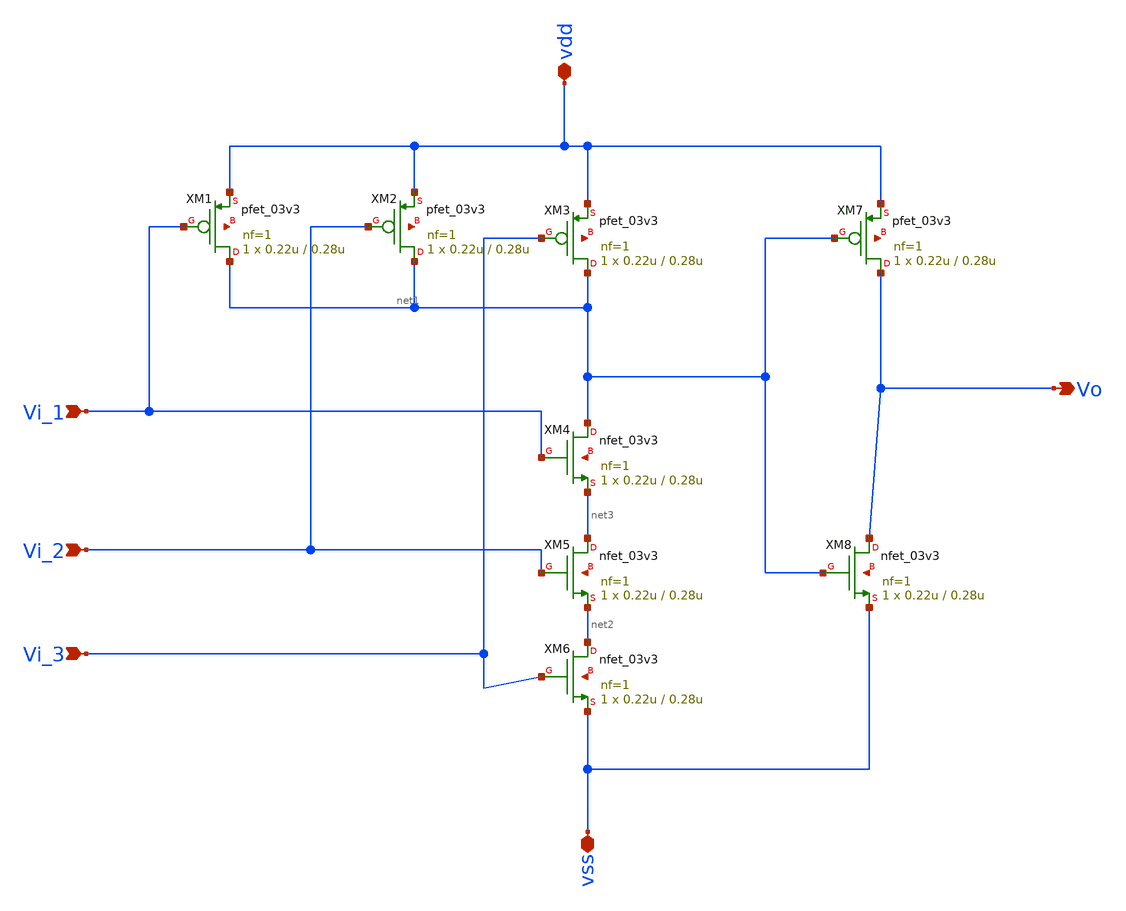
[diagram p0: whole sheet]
** sch_path: designs/3_input_and.sch
**.subckt 3_input_and vdd vss Vi_1 Vi_2 Vi_3 Vo
*.iopin vdd
*.iopin vss
*.ipin Vi_1
*.ipin Vi_2
*.ipin Vi_3
*.opin Vo
XM1 net1 Vi_1 vdd net4 pfet_03v3 L=0.28u W=0.22u nf=1 ad='int((nf+1)/2) * W/nf * 0.18u' as='int((nf+2)/2) * W/nf * 0.18u'
+ pd='2*int((nf+1)/2) * (W/nf + 0.18u)' ps='2*int((nf+2)/2) * (W/nf + 0.18u)' nrd='0.18u / W' nrs='0.18u / W'
+ sa=0 sb=0 sd=0 m=1
XM2 net1 Vi_2 vdd net5 pfet_03v3 L=0.28u W=0.22u nf=1 ad='int((nf+1)/2) * W/nf * 0.18u' as='int((nf+2)/2) * W/nf * 0.18u'
+ pd='2*int((nf+1)/2) * (W/nf + 0.18u)' ps='2*int((nf+2)/2) * (W/nf + 0.18u)' nrd='0.18u / W' nrs='0.18u / W'
+ sa=0 sb=0 sd=0 m=1
XM3 net1 Vi_3 vdd net6 pfet_03v3 L=0.28u W=0.22u nf=1 ad='int((nf+1)/2) * W/nf * 0.18u' as='int((nf+2)/2) * W/nf * 0.18u'
+ pd='2*int((nf+1)/2) * (W/nf + 0.18u)' ps='2*int((nf+2)/2) * (W/nf + 0.18u)' nrd='0.18u / W' nrs='0.18u / W'
+ sa=0 sb=0 sd=0 m=1
XM4 net1 Vi_1 net3 net7 nfet_03v3 L=0.28u W=0.22u nf=1 ad='int((nf+1)/2) * W/nf * 0.18u' as='int((nf+2)/2) * W/nf * 0.18u'
+ pd='2*int((nf+1)/2) * (W/nf + 0.18u)' ps='2*int((nf+2)/2) * (W/nf + 0.18u)' nrd='0.18u / W' nrs='0.18u / W'
+ sa=0 sb=0 sd=0 m=1
XM5 net3 Vi_2 net2 net8 nfet_03v3 L=0.28u W=0.22u nf=1 ad='int((nf+1)/2) * W/nf * 0.18u' as='int((nf+2)/2) * W/nf * 0.18u'
+ pd='2*int((nf+1)/2) * (W/nf + 0.18u)' ps='2*int((nf+2)/2) * (W/nf + 0.18u)' nrd='0.18u / W' nrs='0.18u / W'
+ sa=0 sb=0 sd=0 m=1
XM6 net2 Vi_3 vss net9 nfet_03v3 L=0.28u W=0.22u nf=1 ad='int((nf+1)/2) * W/nf * 0.18u' as='int((nf+2)/2) * W/nf * 0.18u'
+ pd='2*int((nf+1)/2) * (W/nf + 0.18u)' ps='2*int((nf+2)/2) * (W/nf + 0.18u)' nrd='0.18u / W' nrs='0.18u / W'
+ sa=0 sb=0 sd=0 m=1
XM7 Vo net1 vdd net10 pfet_03v3 L=0.28u W=0.22u nf=1 ad='int((nf+1)/2) * W/nf * 0.18u' as='int((nf+2)/2) * W/nf * 0.18u'
+ pd='2*int((nf+1)/2) * (W/nf + 0.18u)' ps='2*int((nf+2)/2) * (W/nf + 0.18u)' nrd='0.18u / W' nrs='0.18u / W'
+ sa=0 sb=0 sd=0 m=1
XM8 Vo net1 vss net11 nfet_03v3 L=0.28u W=0.22u nf=1 ad='int((nf+1)/2) * W/nf * 0.18u' as='int((nf+2)/2) * W/nf * 0.18u'
+ pd='2*int((nf+1)/2) * (W/nf + 0.18u)' ps='2*int((nf+2)/2) * (W/nf + 0.18u)' nrd='0.18u / W' nrs='0.18u / W'
+ sa=0 sb=0 sd=0 m=1
**.ends
.end
